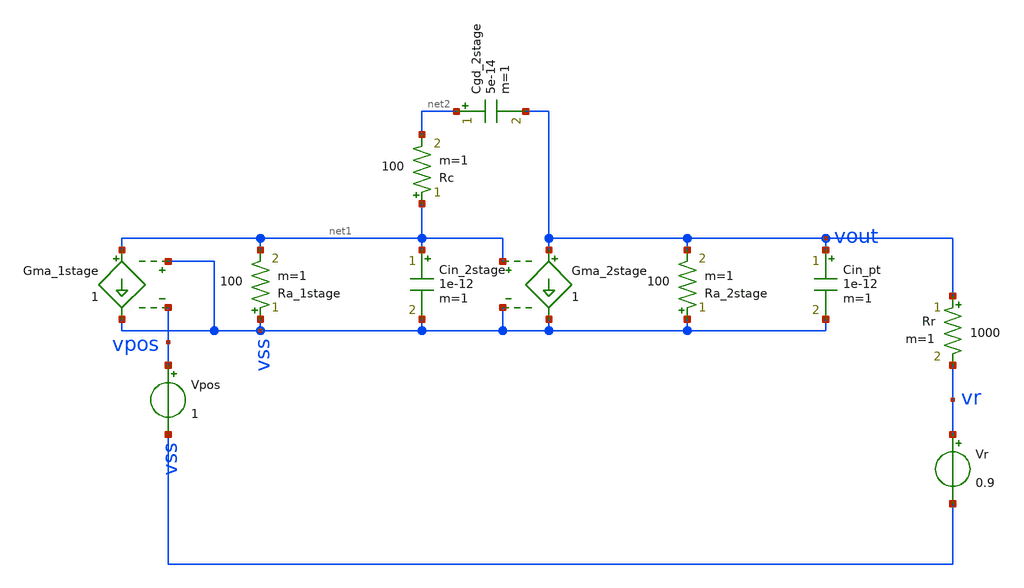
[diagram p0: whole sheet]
** sch_path: test/Tesis_notebooks/xschem/OpAmp_2stage_rout.sch
**.subckt OpAmp_2stage_rout
Gma_1stage net1 vss vss vpos 1
Ra_1stage vss net1 100 m=1
Vpos vpos vss 1
Cin_pt vout vss 1e-12 m=1
Cin_2stage net1 vss 1e-12 m=1
Gma_2stage vout vss net1 vss 1
Ra_2stage vss vout 100 m=1
Cgd_2stage net2 vout 5e-14 m=1
Rc net1 net2 100 m=1
Vr vr vss 0.9
Rr vout vr 1000 m=1
**.ends
.end
